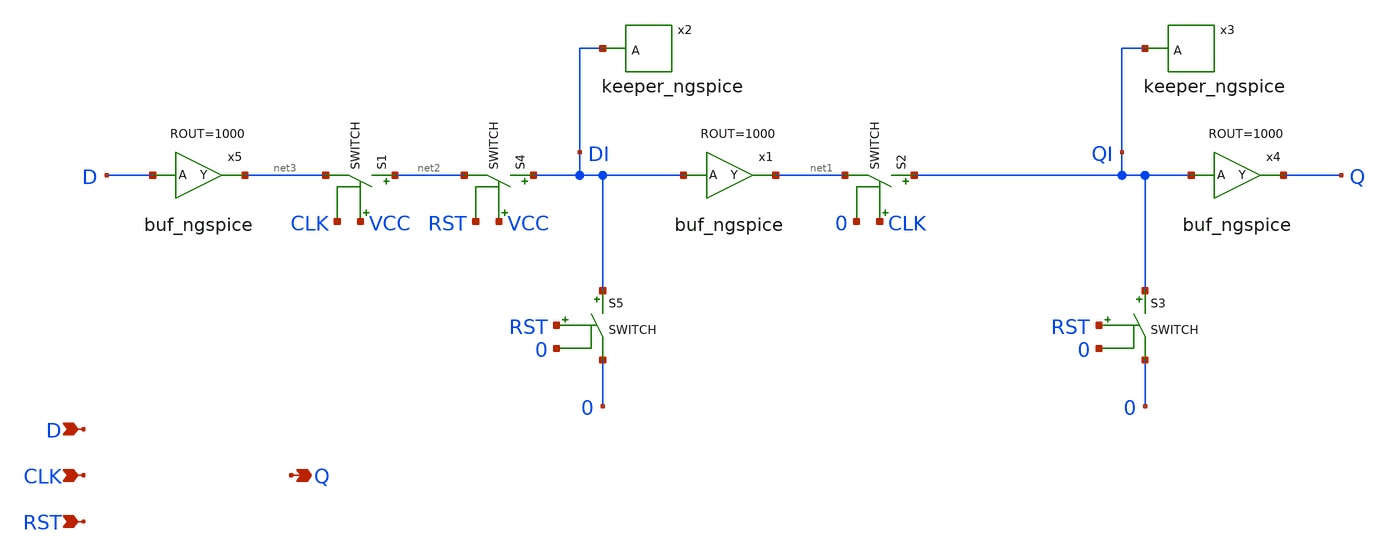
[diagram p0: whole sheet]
** sch_path: xschem_library_oa/ngspice/flip_flop_ngspice/schematic/flip_flop_ngspice.sch
* Copyright (C) 1998-2024 Stefan Frederik Schippers
* This program is free software; you can redistribute it and/or modify
* it under the terms of the GNU General Public License as published by
* the Free Software Foundation; either version 2 of the License, or
* (at your option) any later version.
* This program is distributed in the hope that it will be useful,
* but WITHOUT ANY WARRANTY; without even the implied warranty of
* MERCHANTABILITY or FITNESS FOR A PARTICULAR PURPOSE.  See the
* GNU General Public License for more details.
* You should have received a copy of the GNU General Public License
* along with this program; if not, write to the Free Software
**.subckt flip_flop_ngspice D CLK RST Q
*.ipin D
*.ipin CLK
*.ipin RST
*.opin Q
x2 DI keeper_ngspice
S1 net2 net3 VCC CLK SWITCH
S2 QI net1 CLK 0 SWITCH
x3 QI keeper_ngspice
x4 Q QI buf_ngspice ROUT=1000
S3 QI 0 RST 0 SWITCH
x1 net1 DI buf_ngspice ROUT=1000
S4 DI net2 VCC RST SWITCH
S5 DI 0 RST 0 SWITCH
x5 net3 D buf_ngspice ROUT=1000
**.ends
.end
